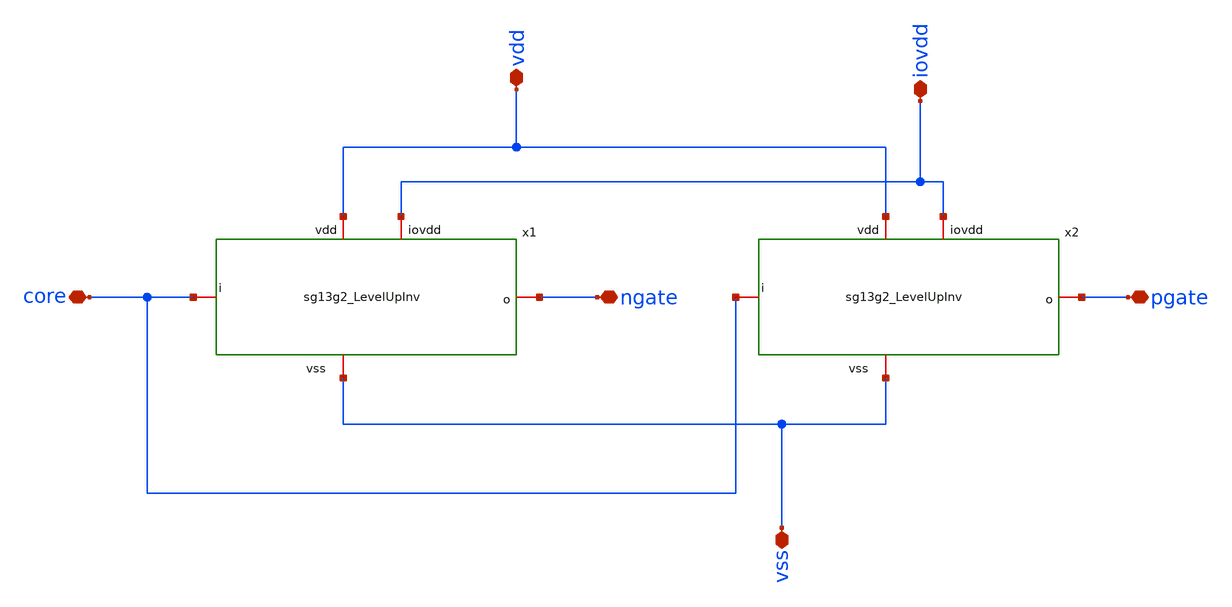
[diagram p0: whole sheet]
** sch_path: design/blocks-std/sg13g2_GateLevelUpInv/schematic/sg13g2_GateLevelUpInv.sch
**.subckt sg13g2_GateLevelUpInv vdd iovdd core vss pgate ngate
*.iopin vdd
*.iopin iovdd
*.iopin core
*.iopin vss
*.iopin pgate
*.iopin ngate
x1 iovdd vdd ngate core vss sg13g2_LevelUpInv
x2 iovdd vdd pgate core vss sg13g2_LevelUpInv
**.ends
.end
